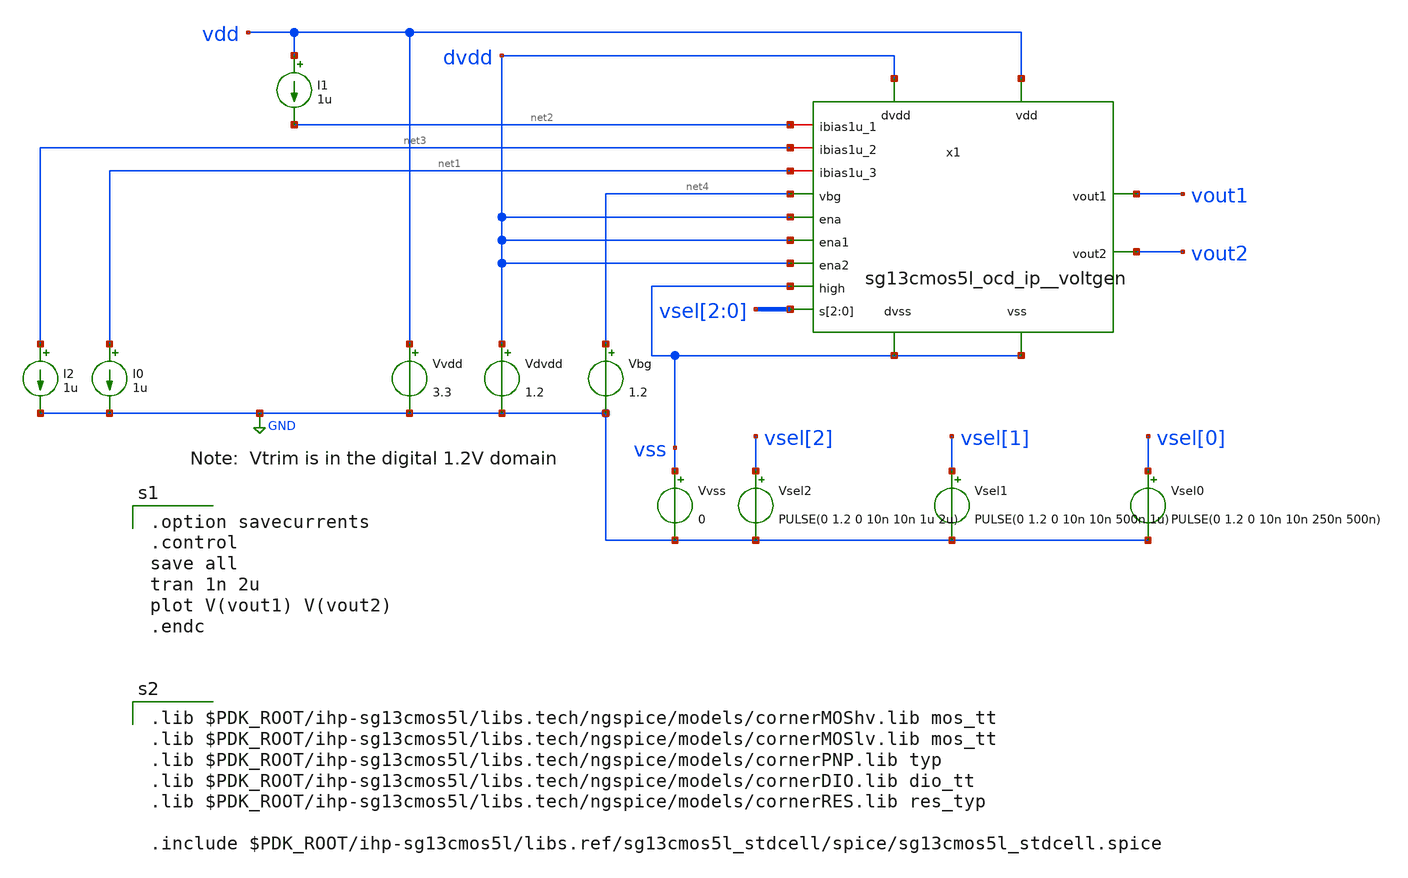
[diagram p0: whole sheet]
** sch_path: xschem/voltgen_tb.sch
**.subckt voltgen_tb
Vvss vss GND 0
Vvdd vdd GND 3.3
I0 net1 GND 1u
Vdvdd dvdd GND 1.2
x1 dvdd vss vdd vsel[2] vsel[1] vsel[0] net4 vss net2 vout2 net3 dvdd vout1 dvdd dvdd net1 vss
+ sg13cmos5l_ocd_ip__voltgen
Vbg net4 GND 1.2
Vsel0 vsel[0] GND PULSE(0 1.2 0 10n 10n 250n 500n)
Vsel1 vsel[1] GND PULSE(0 1.2 0 10n 10n 500n 1u)
Vsel2 vsel[2] GND PULSE(0 1.2 0 10n 10n 1u 2u)
I1 vdd net2 1u
I2 net3 GND 1u
**** begin user architecture code

.option savecurrents
.control
save all
tran 1n 2u
plot V(vout1) V(vout2)
.endc


.lib $PDK_ROOT/ihp-sg13cmos5l/libs.tech/ngspice/models/cornerMOShv.lib mos_tt
.lib $PDK_ROOT/ihp-sg13cmos5l/libs.tech/ngspice/models/cornerMOSlv.lib mos_tt
.lib $PDK_ROOT/ihp-sg13cmos5l/libs.tech/ngspice/models/cornerPNP.lib typ
.lib $PDK_ROOT/ihp-sg13cmos5l/libs.tech/ngspice/models/cornerDIO.lib dio_tt
.lib $PDK_ROOT/ihp-sg13cmos5l/libs.tech/ngspice/models/cornerRES.lib res_typ

.include $PDK_ROOT/ihp-sg13cmos5l/libs.ref/sg13cmos5l_stdcell/spice/sg13cmos5l_stdcell.spice


**** end user architecture code
**.ends
.GLOBAL GND
.end
